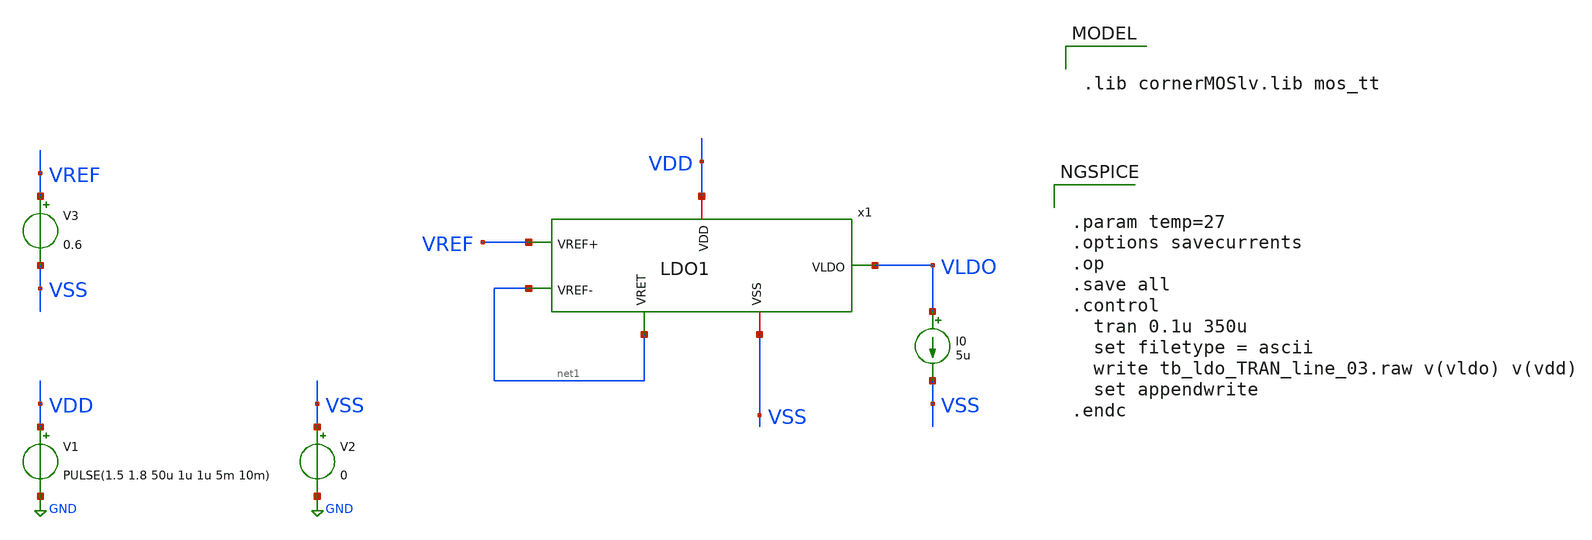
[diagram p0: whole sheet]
** sch_path: designs/1iee34/tb_ldo_TRAN_line.sch
**.subckt tb_ldo_TRAN_line
V1 VDD GND PULSE(1.5 1.8 50u 1u 1u 5m 10m)
V2 VSS GND 0
V3 VREF VSS 0.6
x1 VDD VREF net1 VLDO net1 VSS LDO1
I0 VLDO VSS 5u
**** begin user architecture code


.param temp=27
.options savecurrents
.op
.save all
.control
  tran 0.1u 350u
  set filetype = ascii
  write tb_ldo_TRAN_line_03.raw v(vldo) v(vdd)
  set appendwrite
.endc




.lib cornerMOSlv.lib mos_tt


**** end user architecture code
**.ends

* expanding   symbol:  LDO1.sym # of pins=6
** sym_path: designs/1iee34/LDO1.sym
** sch_path: designs/1iee34/LDO1.sch
.subckt LDO1 VDD VREF+ VREF- VLDO VRET VSS
*.iopin VREF+
*.iopin VLDO
*.iopin VDD
*.iopin VREF-
*.iopin VSS
*.iopin VRET
C1 VLDO VSS 1000.0n m=1
CC net4 net1 3.666349378452877e-05n m=1
R1 VLDO VRET 21.49k m=1
R2 VRET VSS 21.49k m=1
C3 VLDO net5 5n m=1
R3 net1 net5 30k m=1
XMG VLDO net1 VDD VDD sg13_lv_pmos w=250.0u l=0.13u ng=13 m=1 mm_ok=1
XM3 net3 net3 VDD VDD sg13_lv_pmos w=14.74u l=32.58u ng=2 m=1 mm_ok=1
XM4 net4 net3 VDD VDD sg13_lv_pmos w=14.74u l=32.58u ng=2 m=1 mm_ok=1
XM6 net1 net4 VDD VDD sg13_lv_pmos w=3.58u l=1.5u ng=1 m=1 mm_ok=1
XM1 net2 VREF+ net3 VSS sg13_lv_nmos w=176.34u l=8.55u ng=18 m=1 mm_ok=1
XM2 net2 VREF- net4 VSS sg13_lv_nmos w=176.34u l=8.55u ng=18 m=1 mm_ok=1
XM5 VSS VG net2 VSS sg13_lv_nmos w=2.2u l=2.0u ng=1 m=1 mm_ok=1
XM7 VSS VG net1 VSS sg13_lv_nmos w=4.4u l=2.0u ng=1 m=1 mm_ok=1
XM8 VSS VG VG VSS sg13_lv_nmos w=2.75u l=2.0u ng=1 m=1 mm_ok=1
XM10 net6 net6 VDD VDD sg13_lv_pmos w=2u l=8u ng=1 m=1 mm_ok=1
XM11 VG VDD net6 VSS sg13_lv_nmos w=2u l=8u ng=1 m=1 mm_ok=1
.ends

.GLOBAL GND
.end
